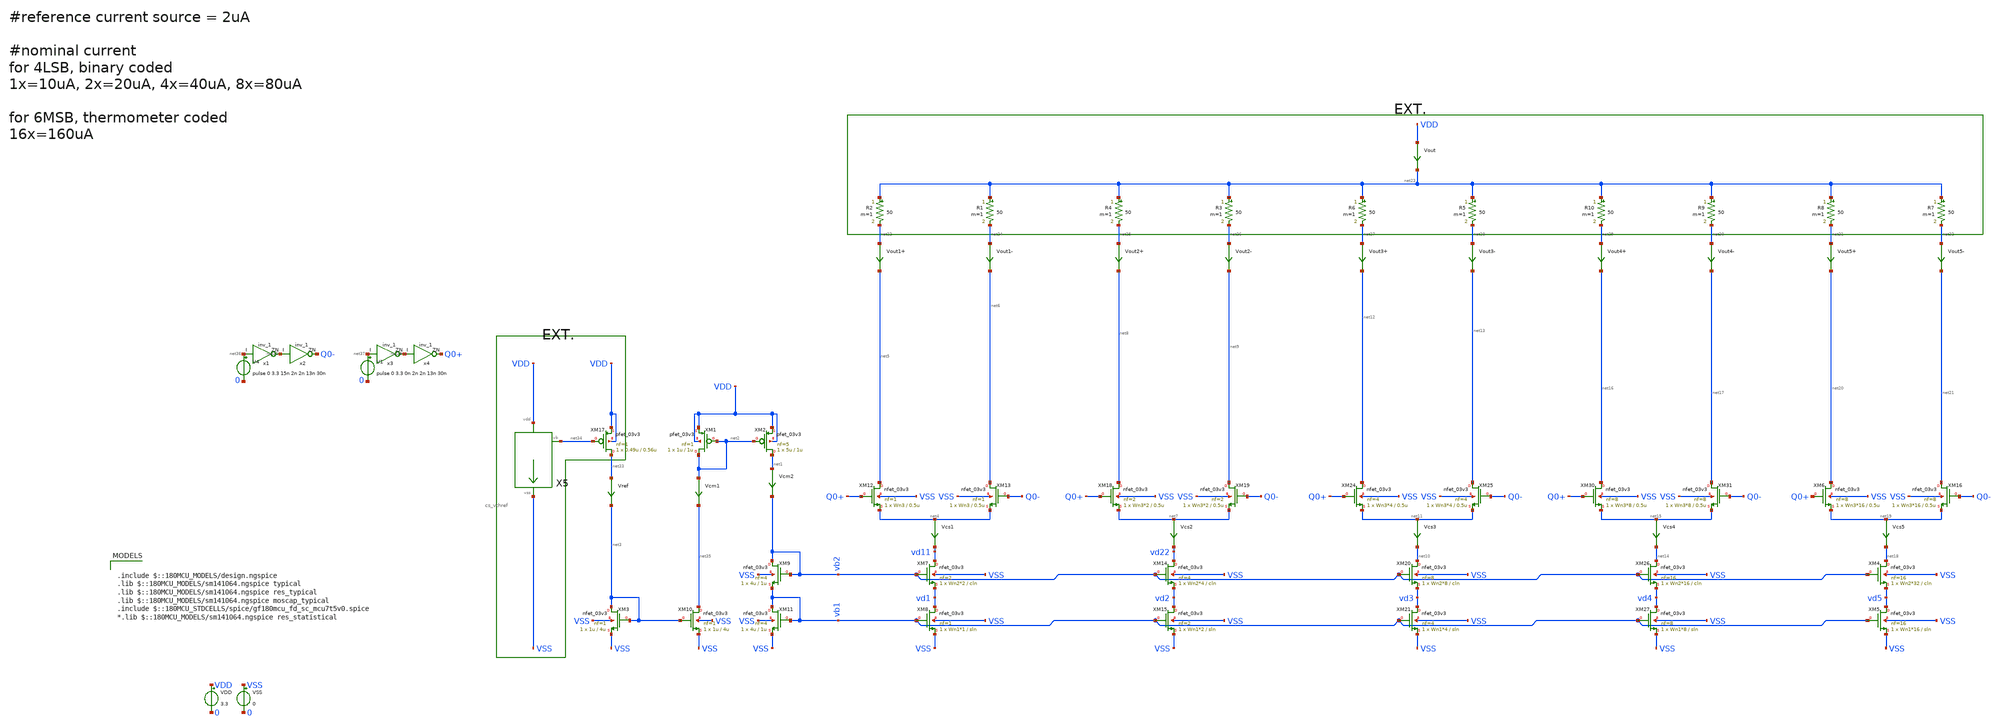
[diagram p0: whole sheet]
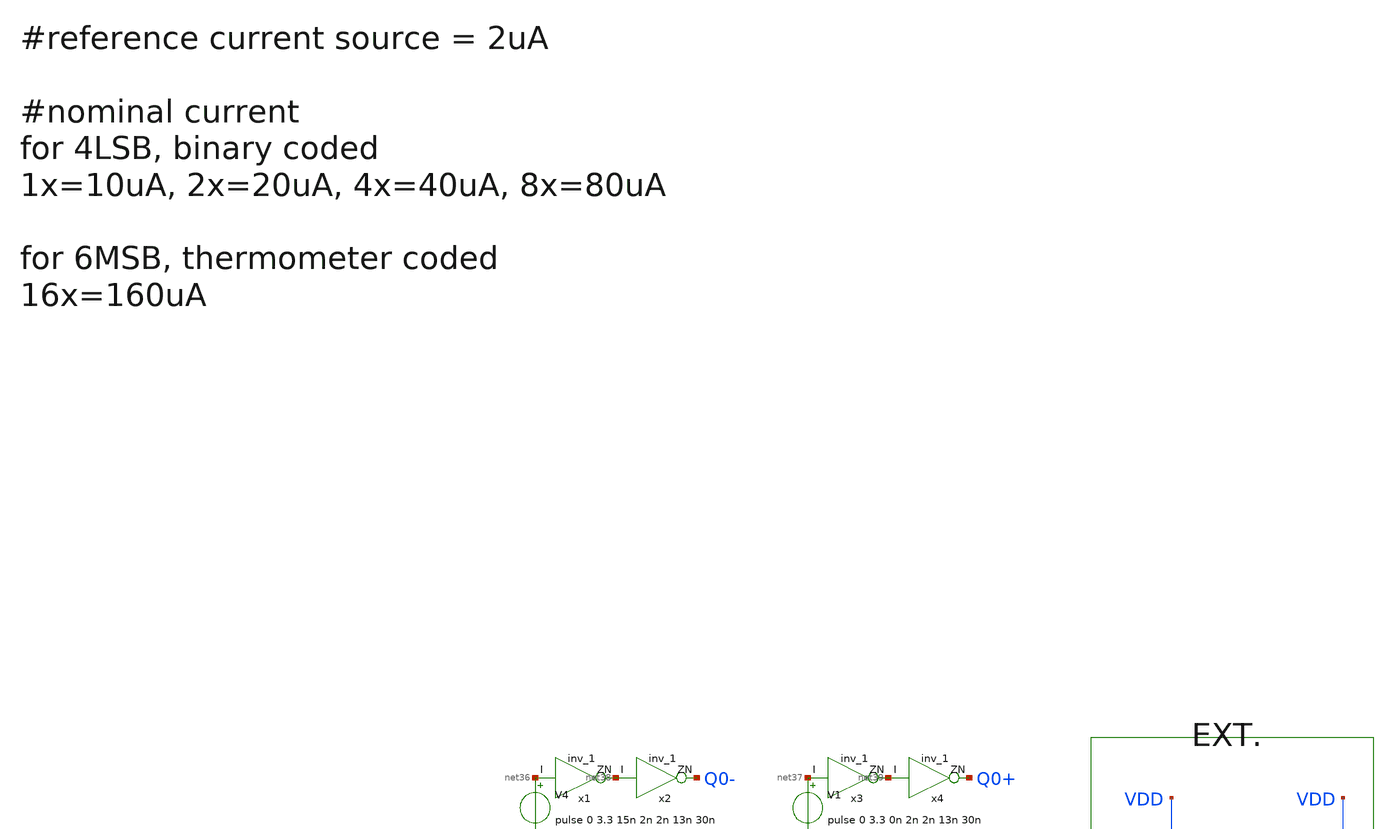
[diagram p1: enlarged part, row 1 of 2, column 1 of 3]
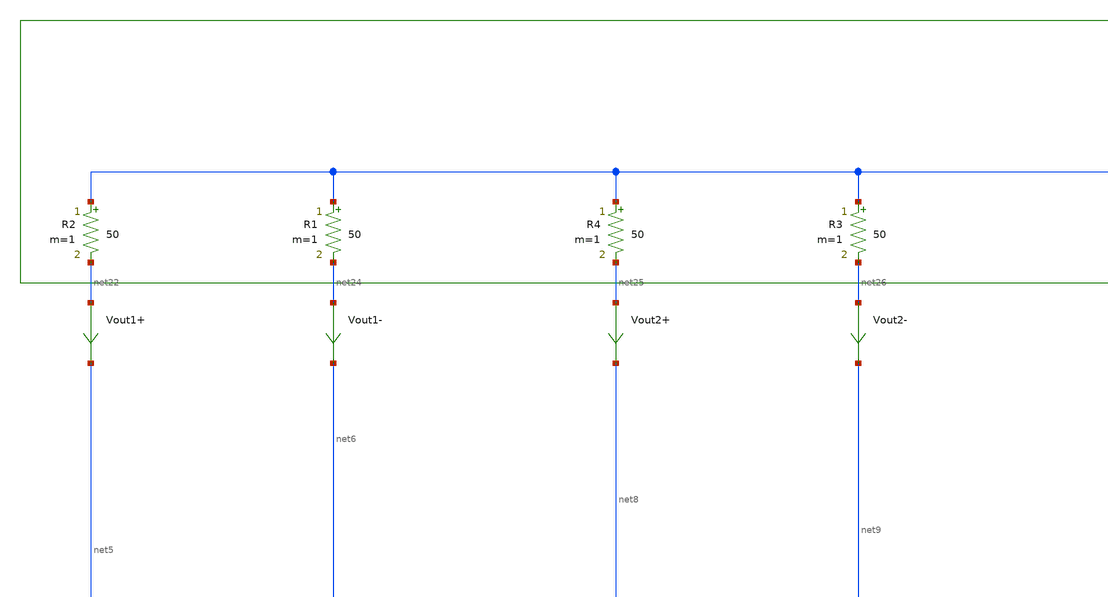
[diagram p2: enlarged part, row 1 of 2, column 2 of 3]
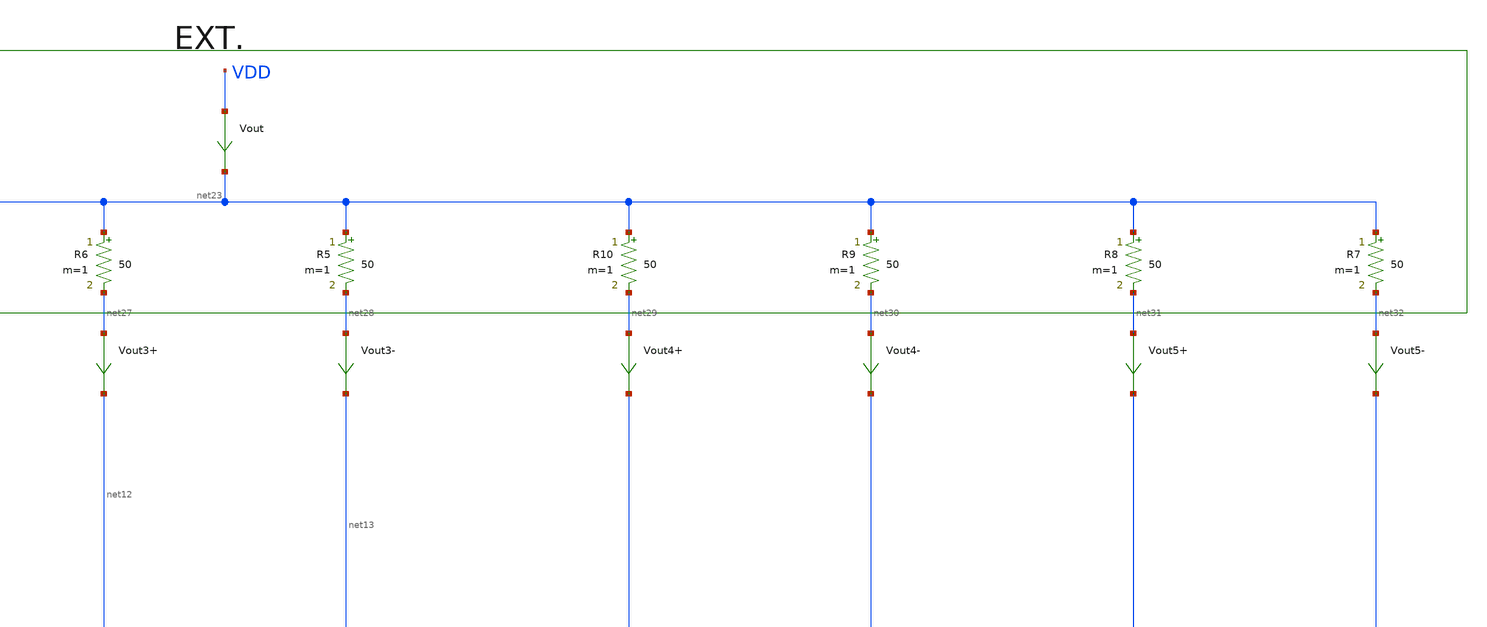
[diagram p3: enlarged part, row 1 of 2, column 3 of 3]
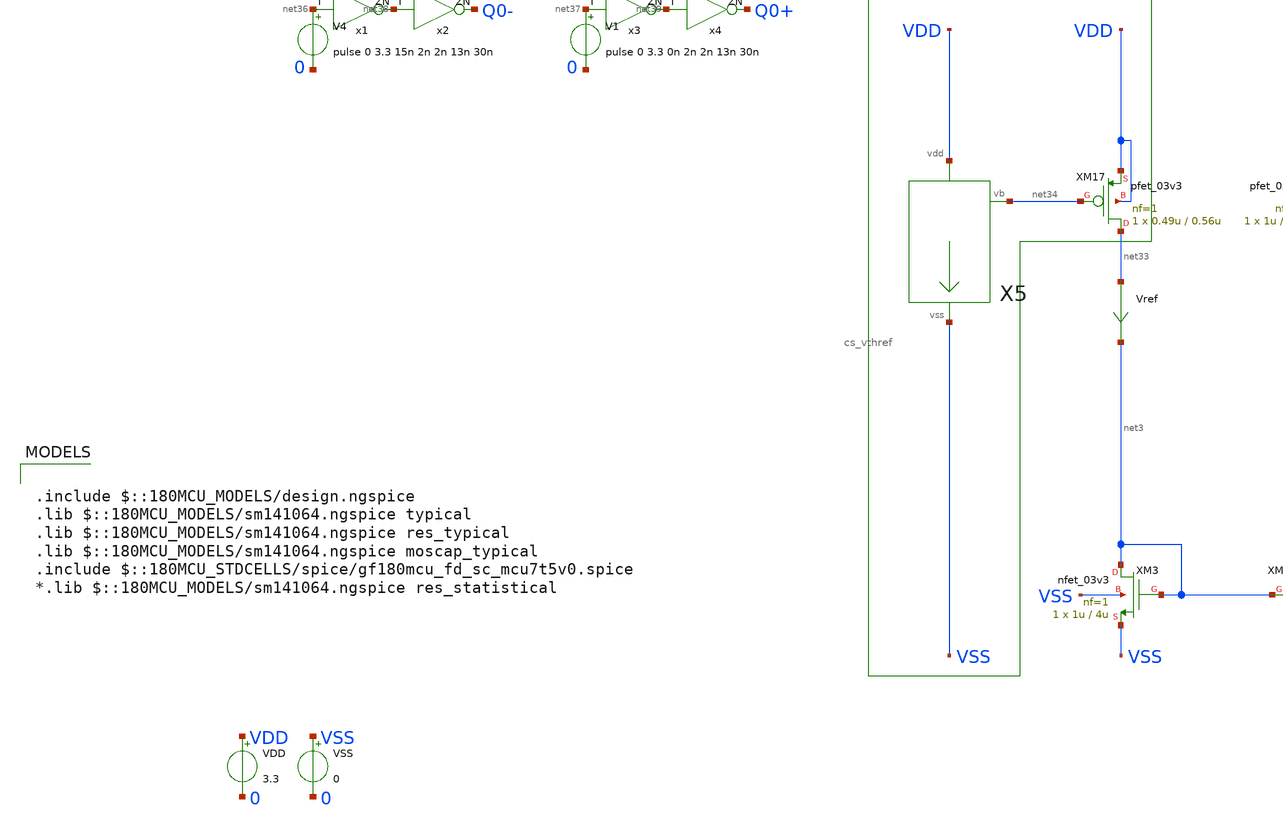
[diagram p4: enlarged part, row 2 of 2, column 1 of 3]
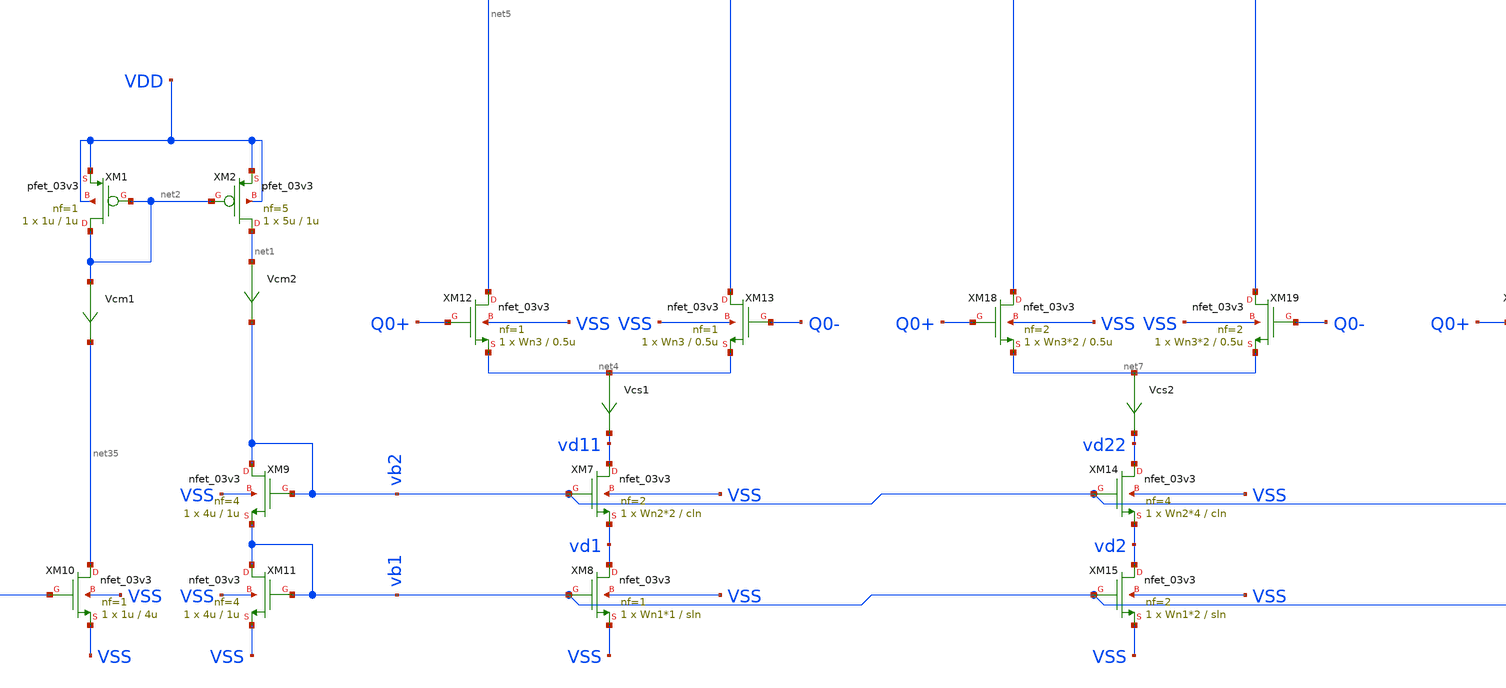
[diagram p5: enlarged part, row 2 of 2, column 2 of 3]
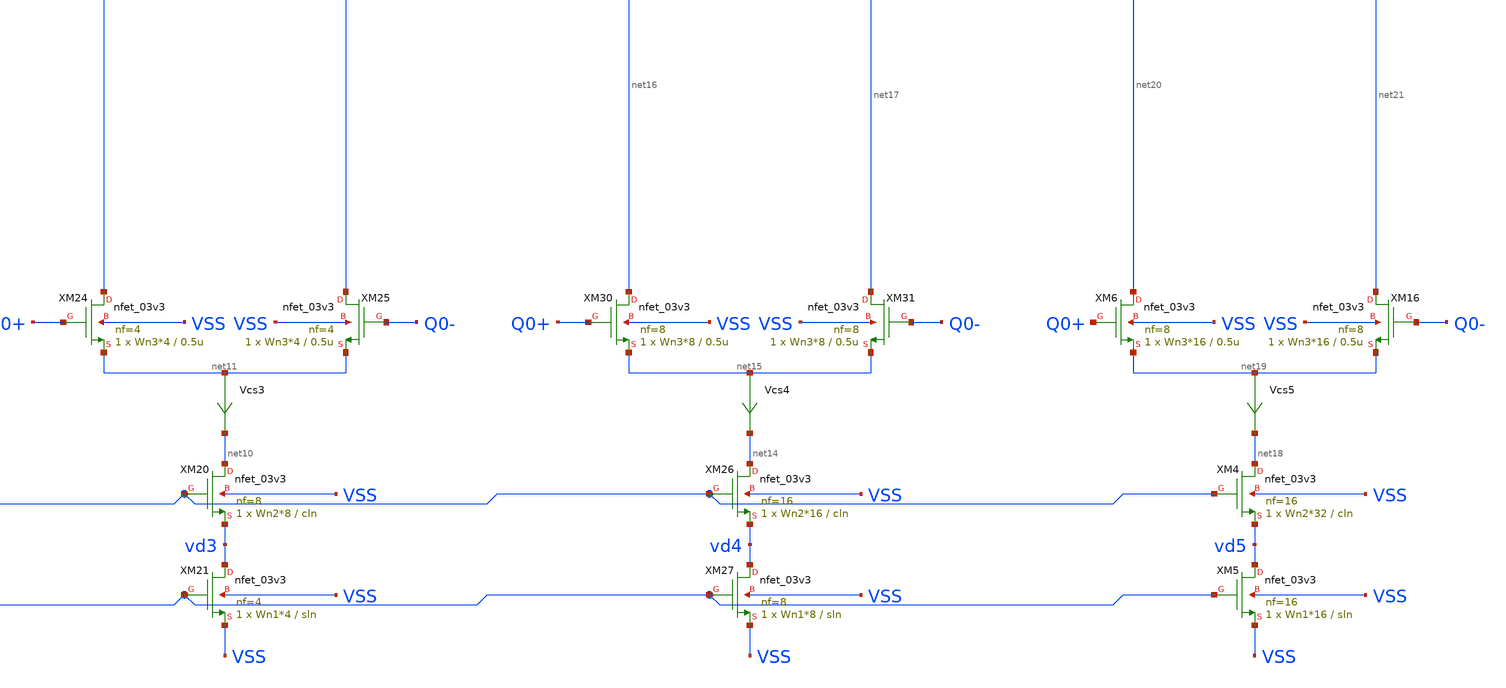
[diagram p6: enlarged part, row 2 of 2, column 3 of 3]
** sch_path: DAC/xschem/dac_device_sizing.sch
**.subckt dac_device_sizing
XM1 net2 net2 VDD VDD pfet_03v3 L=1u W=1u nf=1 ad='int((nf+1)/2) * W/nf * 0.18u' as='int((nf+2)/2) * W/nf * 0.18u'
+ pd='2*int((nf+1)/2) * (W/nf + 0.18u)' ps='2*int((nf+2)/2) * (W/nf + 0.18u)' nrd='0.18u / W' nrs='0.18u / W'
+ sa=0 sb=0 sd=0 m=1
XM2 net1 net2 VDD VDD pfet_03v3 L=1u W=5u nf=5 ad='int((nf+1)/2) * W/nf * 0.18u' as='int((nf+2)/2) * W/nf * 0.18u'
+ pd='2*int((nf+1)/2) * (W/nf + 0.18u)' ps='2*int((nf+2)/2) * (W/nf + 0.18u)' nrd='0.18u / W' nrs='0.18u / W'
+ sa=0 sb=0 sd=0 m=1
XM3 net3 net3 VSS VSS nfet_03v3 L=4u W=1u nf=1 ad='int((nf+1)/2) * W/nf * 0.18u' as='int((nf+2)/2) * W/nf * 0.18u'
+ pd='2*int((nf+1)/2) * (W/nf + 0.18u)' ps='2*int((nf+2)/2) * (W/nf + 0.18u)' nrd='0.18u / W' nrs='0.18u / W'
+ sa=0 sb=0 sd=0 m=1
XM10 net35 net3 VSS VSS nfet_03v3 L=4u W=1u nf=1 ad='int((nf+1)/2) * W/nf * 0.18u' as='int((nf+2)/2) * W/nf * 0.18u'
+ pd='2*int((nf+1)/2) * (W/nf + 0.18u)' ps='2*int((nf+2)/2) * (W/nf + 0.18u)' nrd='0.18u / W' nrs='0.18u / W'
+ sa=0 sb=0 sd=0 m=1
Vref net33 net3 0
.save i(vref)
XM7 vd11 vb2 vd1 VSS nfet_03v3 L=cln W=Wn2*2 nf=2 ad='int((nf+1)/2) * W/nf * 0.18u' as='int((nf+2)/2) * W/nf * 0.18u'
+ pd='2*int((nf+1)/2) * (W/nf + 0.18u)' ps='2*int((nf+2)/2) * (W/nf + 0.18u)' nrd='0.18u / W' nrs='0.18u / W'
+ sa=0 sb=0 sd=0 m=1
XM8 vd1 vb1 VSS VSS nfet_03v3 L=sln W=Wn1*1 nf=1 ad='int((nf+1)/2) * W/nf * 0.18u' as='int((nf+2)/2) * W/nf * 0.18u'
+ pd='2*int((nf+1)/2) * (W/nf + 0.18u)' ps='2*int((nf+2)/2) * (W/nf + 0.18u)' nrd='0.18u / W' nrs='0.18u / W'
+ sa=0 sb=0 sd=0 m=1
XM9 vb2 vb2 vb1 VSS nfet_03v3 L=1u W=4u nf=4 ad='int((nf+1)/2) * W/nf * 0.18u' as='int((nf+2)/2) * W/nf * 0.18u'
+ pd='2*int((nf+1)/2) * (W/nf + 0.18u)' ps='2*int((nf+2)/2) * (W/nf + 0.18u)' nrd='0.18u / W' nrs='0.18u / W'
+ sa=0 sb=0 sd=0 m=1
XM11 vb1 vb1 VSS VSS nfet_03v3 L=1u W=4u nf=4 ad='int((nf+1)/2) * W/nf * 0.18u' as='int((nf+2)/2) * W/nf * 0.18u'
+ pd='2*int((nf+1)/2) * (W/nf + 0.18u)' ps='2*int((nf+2)/2) * (W/nf + 0.18u)' nrd='0.18u / W' nrs='0.18u / W'
+ sa=0 sb=0 sd=0 m=1
XM12 net5 Q0+ net4 VSS nfet_03v3 L=0.5u W=Wn3 nf=1 ad='int((nf+1)/2) * W/nf * 0.18u' as='int((nf+2)/2) * W/nf * 0.18u'
+ pd='2*int((nf+1)/2) * (W/nf + 0.18u)' ps='2*int((nf+2)/2) * (W/nf + 0.18u)' nrd='0.18u / W' nrs='0.18u / W'
+ sa=0 sb=0 sd=0 m=1
XM13 net6 Q0- net4 VSS nfet_03v3 L=0.5u W=Wn3 nf=1 ad='int((nf+1)/2) * W/nf * 0.18u' as='int((nf+2)/2) * W/nf * 0.18u'
+ pd='2*int((nf+1)/2) * (W/nf + 0.18u)' ps='2*int((nf+2)/2) * (W/nf + 0.18u)' nrd='0.18u / W' nrs='0.18u / W'
+ sa=0 sb=0 sd=0 m=1
Vcm1 net2 net35 0
.save i(vcm1)
Vcm2 net1 vb2 0
.save i(vcm2)
Vcs1 net4 vd11 0
.save i(vcs1)
XM14 vd22 vb2 vd2 VSS nfet_03v3 L=cln W=Wn2*4 nf=4 ad='int((nf+1)/2) * W/nf * 0.18u' as='int((nf+2)/2) * W/nf * 0.18u'
+ pd='2*int((nf+1)/2) * (W/nf + 0.18u)' ps='2*int((nf+2)/2) * (W/nf + 0.18u)' nrd='0.18u / W' nrs='0.18u / W'
+ sa=0 sb=0 sd=0 m=1
XM15 vd2 vb1 VSS VSS nfet_03v3 L=sln W=Wn1*2 nf=2 ad='int((nf+1)/2) * W/nf * 0.18u' as='int((nf+2)/2) * W/nf * 0.18u'
+ pd='2*int((nf+1)/2) * (W/nf + 0.18u)' ps='2*int((nf+2)/2) * (W/nf + 0.18u)' nrd='0.18u / W' nrs='0.18u / W'
+ sa=0 sb=0 sd=0 m=1
XM18 net8 Q0+ net7 VSS nfet_03v3 L=0.5u W=Wn3*2 nf=2 ad='int((nf+1)/2) * W/nf * 0.18u' as='int((nf+2)/2) * W/nf * 0.18u'
+ pd='2*int((nf+1)/2) * (W/nf + 0.18u)' ps='2*int((nf+2)/2) * (W/nf + 0.18u)' nrd='0.18u / W' nrs='0.18u / W'
+ sa=0 sb=0 sd=0 m=1
XM19 net9 Q0- net7 VSS nfet_03v3 L=0.5u W=Wn3*2 nf=2 ad='int((nf+1)/2) * W/nf * 0.18u' as='int((nf+2)/2) * W/nf * 0.18u'
+ pd='2*int((nf+1)/2) * (W/nf + 0.18u)' ps='2*int((nf+2)/2) * (W/nf + 0.18u)' nrd='0.18u / W' nrs='0.18u / W'
+ sa=0 sb=0 sd=0 m=1
Vout1+ net22 net5 0
.save i(vout1+)
Vout1- net24 net6 0
.save i(vout1-)
XM20 net10 vb2 vd3 VSS nfet_03v3 L=cln W=Wn2*8 nf=8 ad='int((nf+1)/2) * W/nf * 0.18u' as='int((nf+2)/2) * W/nf * 0.18u'
+ pd='2*int((nf+1)/2) * (W/nf + 0.18u)' ps='2*int((nf+2)/2) * (W/nf + 0.18u)' nrd='0.18u / W' nrs='0.18u / W'
+ sa=0 sb=0 sd=0 m=1
XM21 vd3 vb1 VSS VSS nfet_03v3 L=sln W=Wn1*4 nf=4 ad='int((nf+1)/2) * W/nf * 0.18u' as='int((nf+2)/2) * W/nf * 0.18u'
+ pd='2*int((nf+1)/2) * (W/nf + 0.18u)' ps='2*int((nf+2)/2) * (W/nf + 0.18u)' nrd='0.18u / W' nrs='0.18u / W'
+ sa=0 sb=0 sd=0 m=1
XM24 net12 Q0+ net11 VSS nfet_03v3 L=0.5u W=Wn3*4 nf=4 ad='int((nf+1)/2) * W/nf * 0.18u' as='int((nf+2)/2) * W/nf * 0.18u'
+ pd='2*int((nf+1)/2) * (W/nf + 0.18u)' ps='2*int((nf+2)/2) * (W/nf + 0.18u)' nrd='0.18u / W' nrs='0.18u / W'
+ sa=0 sb=0 sd=0 m=1
XM25 net13 Q0- net11 VSS nfet_03v3 L=0.5u W=Wn3*4 nf=4 ad='int((nf+1)/2) * W/nf * 0.18u' as='int((nf+2)/2) * W/nf * 0.18u'
+ pd='2*int((nf+1)/2) * (W/nf + 0.18u)' ps='2*int((nf+2)/2) * (W/nf + 0.18u)' nrd='0.18u / W' nrs='0.18u / W'
+ sa=0 sb=0 sd=0 m=1
XM26 net14 vb2 vd4 VSS nfet_03v3 L=cln W=Wn2*16 nf=16 ad='int((nf+1)/2) * W/nf * 0.18u' as='int((nf+2)/2) * W/nf * 0.18u'
+ pd='2*int((nf+1)/2) * (W/nf + 0.18u)' ps='2*int((nf+2)/2) * (W/nf + 0.18u)' nrd='0.18u / W' nrs='0.18u / W'
+ sa=0 sb=0 sd=0 m=1
XM27 vd4 vb1 VSS VSS nfet_03v3 L=sln W=Wn1*8 nf=8 ad='int((nf+1)/2) * W/nf * 0.18u' as='int((nf+2)/2) * W/nf * 0.18u'
+ pd='2*int((nf+1)/2) * (W/nf + 0.18u)' ps='2*int((nf+2)/2) * (W/nf + 0.18u)' nrd='0.18u / W' nrs='0.18u / W'
+ sa=0 sb=0 sd=0 m=1
XM30 net16 Q0+ net15 VSS nfet_03v3 L=0.5u W=Wn3*8 nf=8 ad='int((nf+1)/2) * W/nf * 0.18u' as='int((nf+2)/2) * W/nf * 0.18u'
+ pd='2*int((nf+1)/2) * (W/nf + 0.18u)' ps='2*int((nf+2)/2) * (W/nf + 0.18u)' nrd='0.18u / W' nrs='0.18u / W'
+ sa=0 sb=0 sd=0 m=1
XM31 net17 Q0- net15 VSS nfet_03v3 L=0.5u W=Wn3*8 nf=8 ad='int((nf+1)/2) * W/nf * 0.18u' as='int((nf+2)/2) * W/nf * 0.18u'
+ pd='2*int((nf+1)/2) * (W/nf + 0.18u)' ps='2*int((nf+2)/2) * (W/nf + 0.18u)' nrd='0.18u / W' nrs='0.18u / W'
+ sa=0 sb=0 sd=0 m=1
VDD VDD 0 3.3
VSS VSS 0 0
V4 net36 0 pulse 0 3.3 15n 2n 2n 13n 30n
V1 net37 0 pulse 0 3.3 0n 2n 2n 13n 30n
x1 net36 net38 VDD VNW VPW VSS gf180mcu_fd_sc_mcu7t5v0__inv_1
x2 net38 Q0- VDD VNW VPW VSS gf180mcu_fd_sc_mcu7t5v0__inv_1
x3 net37 net39 VDD VNW VPW VSS gf180mcu_fd_sc_mcu7t5v0__inv_1
x4 net39 Q0+ VDD VNW VPW VSS gf180mcu_fd_sc_mcu7t5v0__inv_1
XM4 net18 vb2 vd5 VSS nfet_03v3 L=cln W=Wn2*32 nf=16 ad='int((nf+1)/2) * W/nf * 0.18u' as='int((nf+2)/2) * W/nf * 0.18u'
+ pd='2*int((nf+1)/2) * (W/nf + 0.18u)' ps='2*int((nf+2)/2) * (W/nf + 0.18u)' nrd='0.18u / W' nrs='0.18u / W'
+ sa=0 sb=0 sd=0 m=1
XM5 vd5 vb1 VSS VSS nfet_03v3 L=sln W=Wn1*16 nf=16 ad='int((nf+1)/2) * W/nf * 0.18u' as='int((nf+2)/2) * W/nf * 0.18u'
+ pd='2*int((nf+1)/2) * (W/nf + 0.18u)' ps='2*int((nf+2)/2) * (W/nf + 0.18u)' nrd='0.18u / W' nrs='0.18u / W'
+ sa=0 sb=0 sd=0 m=1
XM6 net20 Q0+ net19 VSS nfet_03v3 L=0.5u W=Wn3*16 nf=8 ad='int((nf+1)/2) * W/nf * 0.18u' as='int((nf+2)/2) * W/nf * 0.18u'
+ pd='2*int((nf+1)/2) * (W/nf + 0.18u)' ps='2*int((nf+2)/2) * (W/nf + 0.18u)' nrd='0.18u / W' nrs='0.18u / W'
+ sa=0 sb=0 sd=0 m=1
XM16 net21 Q0- net19 VSS nfet_03v3 L=0.5u W=Wn3*16 nf=8 ad='int((nf+1)/2) * W/nf * 0.18u' as='int((nf+2)/2) * W/nf * 0.18u'
+ pd='2*int((nf+1)/2) * (W/nf + 0.18u)' ps='2*int((nf+2)/2) * (W/nf + 0.18u)' nrd='0.18u / W' nrs='0.18u / W'
+ sa=0 sb=0 sd=0 m=1
Vcs2 net7 vd22 0
.save i(vcs2)
Vcs3 net11 net10 0
.save i(vcs3)
Vcs4 net15 net14 0
.save i(vcs4)
Vcs5 net19 net18 0
.save i(vcs5)
R1 net23 net24 50 m=1
R2 net23 net22 50 m=1
R3 net23 net26 50 m=1
R4 net23 net25 50 m=1
R5 net23 net28 50 m=1
R6 net23 net27 50 m=1
R9 net23 net30 50 m=1
R10 net23 net29 50 m=1
R7 net23 net32 50 m=1
R8 net23 net31 50 m=1
X5 VSS VDD net34 cs_vthref
XM17 net33 net34 VDD VDD pfet_03v3 L=0.56u W=0.49u nf=1 ad='int((nf+1)/2) * W/nf * 0.18u' as='int((nf+2)/2) * W/nf * 0.18u'
+ pd='2*int((nf+1)/2) * (W/nf + 0.18u)' ps='2*int((nf+2)/2) * (W/nf + 0.18u)' nrd='0.18u / W' nrs='0.18u / W'
+ sa=0 sb=0 sd=0 m=1
Vout2+ net25 net8 0
.save i(vout2+)
Vout2- net26 net9 0
.save i(vout2-)
Vout3+ net27 net12 0
.save i(vout3+)
Vout3- net28 net13 0
.save i(vout3-)
Vout4+ net29 net16 0
.save i(vout4+)
Vout4- net30 net17 0
.save i(vout4-)
Vout5+ net31 net20 0
.save i(vout5+)
Vout5- net32 net21 0
.save i(vout5-)
Vout VDD net23 0
.save i(vout)
**** begin user architecture code


.param Mn1=1
.param Mn2=1
.param Mn3=1
.param Mn4=1
.param nf1=1
.param nf2=2
.param nf3=3
.param nf4=4
.param sln=0.5u
.param cln=0.5u
.param Wn1=2u
.param Wn2=1u
.param Wn3=1u

.save @m.xm7.m0[vth] @m.xm8.m0[vth] @m.xm27.m0[vth] @m.xm26.m0[vth] @m.xm30.m0[vth]
.options savecurrents

.control
	tran 0.5n 100n

	****plot currents of each current mirrror*****
	plot i(Vref) i(Vcm1) i(Vcm2)
	****plot currents of each current source****
	plot i(vcs1) i(Vcs2) i(Vcs3) i(Vcs4) i(Vcs5)
	****plot output currents of each cell****
	plot i(Vout1+) i(Vout1-) i(Vout2+) i(Vout2-) i(Vout3+) i(Vout3-) i(Vout4+) i(Vout4-) i(Vout5+)
+ i(Vout5-)

	*plot i(Vmeas1) i(Vmeas2) i(Vmeas3) i(Vmeas4) i(Vmeas5)
	*plot v(vb2) v(vb1) v(vd1) v(vd2)
	*plot v(vb1)-@m.xm8.m0[vth]
	*plot v(vb2)-@m.xm8.m0[vth]
	*plot v(vb1)-@m.xm8.m0[vth]
	*plot v(vb2)-v(vd1)-@m.xm7.m0[vth]
	*plot v(q0+)-v(vd2)-@m.xm12.m0[vth]
	*plot v(vb1)-@m.xm27.m0[vth]
	*plot v(q0+)-v(vd2)-@m.xm12.m0[vth]
	*plot @m.xm8.m0[vth] @m.xm27.m0[vth]
	*plot v(vd1)-v(vb1)+@m.xm8.m0[vth]
	*plot v(vd1)-v(vb1)+@m.xm15.m0[vth]
	*plot v(vd1)-v(vb1)+@m.xm21.m0[vth]
	*plot v(vd1)-v(vb1)+@m.xm27.m0[vth]
	*plot v(vd1)-v(vb1)+@m.xm5.m0[vth]
	*plot v(vd11)-v(vb2)+@m.xm8.m0[vth]
	*plot v(vb1) v(vd1) v(vd2) v(vd3) v(vd4) v(vd5)
	*plot v(vb1) v(vd1) v(vd2) v(vd3) v(vd4) v(vd5)
	write tb_mosfet_sizing.raw
.endc

.save all



.include $::180MCU_MODELS/design.ngspice
.lib $::180MCU_MODELS/sm141064.ngspice typical
.lib $::180MCU_MODELS/sm141064.ngspice res_typical
.lib $::180MCU_MODELS/sm141064.ngspice moscap_typical
.include $::180MCU_STDCELLS/spice/gf180mcu_fd_sc_mcu7t5v0.spice
*.lib $::180MCU_MODELS/sm141064.ngspice res_statistical

**** end user architecture code
**.ends
.end
